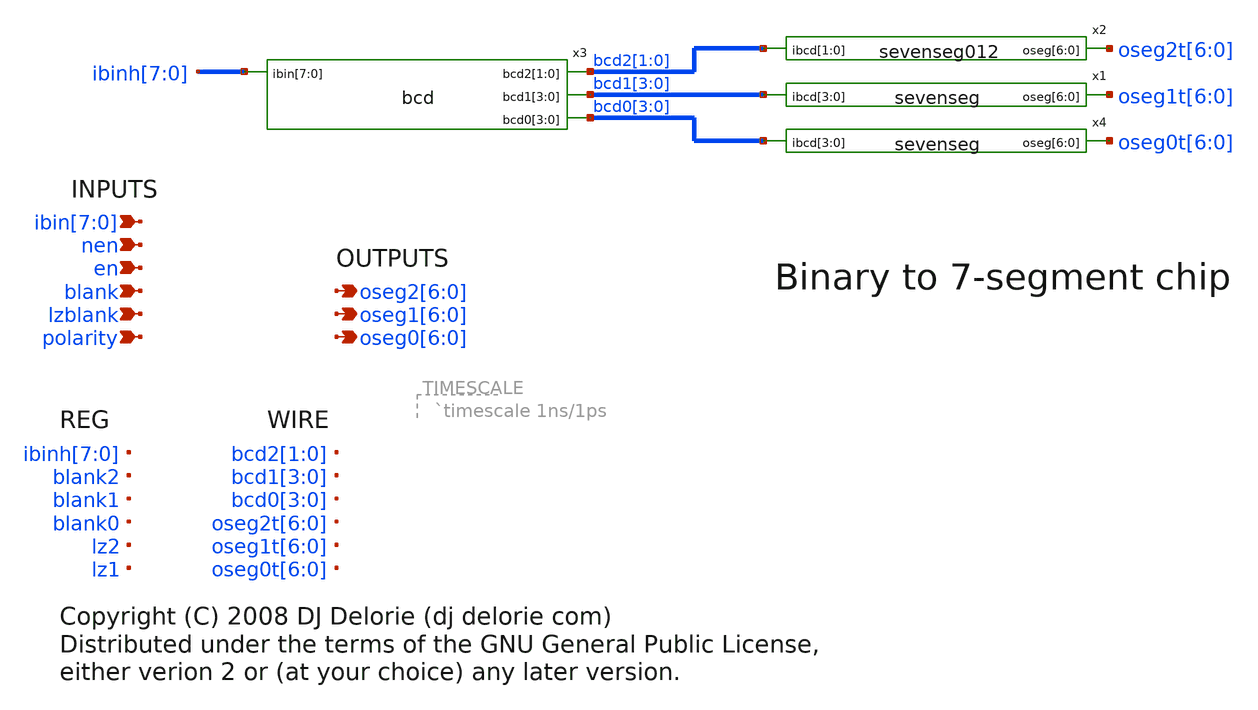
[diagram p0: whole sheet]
** sch_path: xschem_library/binto7seg/top.sch
**.subckt top nen en blank polarity lzblank
*+ ibin[7],ibin[6],ibin[5],ibin[4],ibin[3],ibin[2],ibin[1],ibin[0] oseg2[6],oseg2[5],oseg2[4],oseg2[3],oseg2[2],oseg2[1],oseg2[0]
*+ oseg1[6],oseg1[5],oseg1[4],oseg1[3],oseg1[2],oseg1[1],oseg1[0] oseg0[6],oseg0[5],oseg0[4],oseg0[3],oseg0[2],oseg0[1],oseg0[0]
*.ipin nen
*.ipin en
*.ipin blank
*.ipin polarity
*.ipin lzblank
*.ipin ibin[7],ibin[6],ibin[5],ibin[4],ibin[3],ibin[2],ibin[1],ibin[0]
*.opin oseg2[6],oseg2[5],oseg2[4],oseg2[3],oseg2[2],oseg2[1],oseg2[0]
*.opin oseg1[6],oseg1[5],oseg1[4],oseg1[3],oseg1[2],oseg1[1],oseg1[0]
*.opin oseg0[6],oseg0[5],oseg0[4],oseg0[3],oseg0[2],oseg0[1],oseg0[0]
x1 oseg1t[6] oseg1t[5] oseg1t[4] oseg1t[3] oseg1t[2] oseg1t[1] oseg1t[0] bcd1[3] bcd1[2] bcd1[1]
+ bcd1[0] sevenseg
x2 oseg2t[6] oseg2t[5] oseg2t[4] oseg2t[3] oseg2t[2] oseg2t[1] oseg2t[0] bcd2[1] bcd2[0] sevenseg012
x3 bcd2[1] bcd2[0] ibinh[7] ibinh[6] ibinh[5] ibinh[4] ibinh[3] ibinh[2] ibinh[1] ibinh[0] bcd1[3]
+ bcd1[2] bcd1[1] bcd1[0] bcd0[3] bcd0[2] bcd0[1] bcd0[0] bcd
x4 oseg0t[6] oseg0t[5] oseg0t[4] oseg0t[3] oseg0t[2] oseg0t[1] oseg0t[0] bcd0[3] bcd0[2] bcd0[1]
+ bcd0[0] sevenseg
**** begin user architecture code

// Copyright (C) 2008 DJ Delorie <dj delorie com>
// Distributed under the terms of the GNU General Public License,
// either verion 2 or (at your choice) any later version.

always @ (ibin, nen, en)
begin
  if (en & ~ nen)
    ibinh = ibin;
  else
    ibinh = ibinh;
end


always @ (bcd2, bcd1)
begin
  lz2 = (bcd2 == 0) ? 1 : 0;
  lz1 = (bcd1 == 0) ? lz2 : 0;
end

always @ (lz2, lz1, lzblank, blank)
begin
  blank2 = (lzblank & lz2) | blank;
  blank1 = (lzblank & lz1) | blank;
  blank0 = blank;
end

always @ (oseg2t, polarity, blank2)
begin
  if (blank2)
    oseg2 = 7'bZ;
  else if (polarity)
    oseg2 = ~ oseg2t;
  else
    oseg2 = oseg2t;
end

always @ (oseg1t, polarity, blank1, blank2)
begin
  if (blank1)
    oseg1 = 7'bZ;
  else if (polarity)
    oseg1 = ~ oseg1t;
  else
    oseg1 = oseg1t;
end

always @ (oseg0t, polarity, blank0)
begin
  if (blank0)
    oseg0 = 7'bZ;
  else if (polarity)
    oseg0 = ~ oseg0t;
  else
    oseg0 = oseg0t;
end




reg [7:0] iibin;
reg ien;
reg inen;
reg iblank;
reg ilzblank;
reg ipolarity;

initial begin
  $dumpfile("dumpfile.vcd");
  $dumpvars;
end

task binpattern;
begin
  iibin = 0;
  #100;
  iibin = 1;
  #100;
  iibin = 2;
  #100;
  iibin = 234;
  #100;
  iibin = 255;
  #100;
  iibin = 188;
  #100;
  iibin = 222;
  #100;
end endtask

initial begin
  ien = 1;
  inen = 0;
  iblank = 0;
  ilzblank = 0;
  ipolarity = 0;
  binpattern;
  ilzblank = 1; // blank leading zeros
  binpattern;
end

assign en = ien;
assign nen = inen;
assign ibin = iibin;
assign blank = iblank;
assign lzblank = ilzblank;
assign polarity = ipolarity;


**** end user architecture code
**.ends
.end
